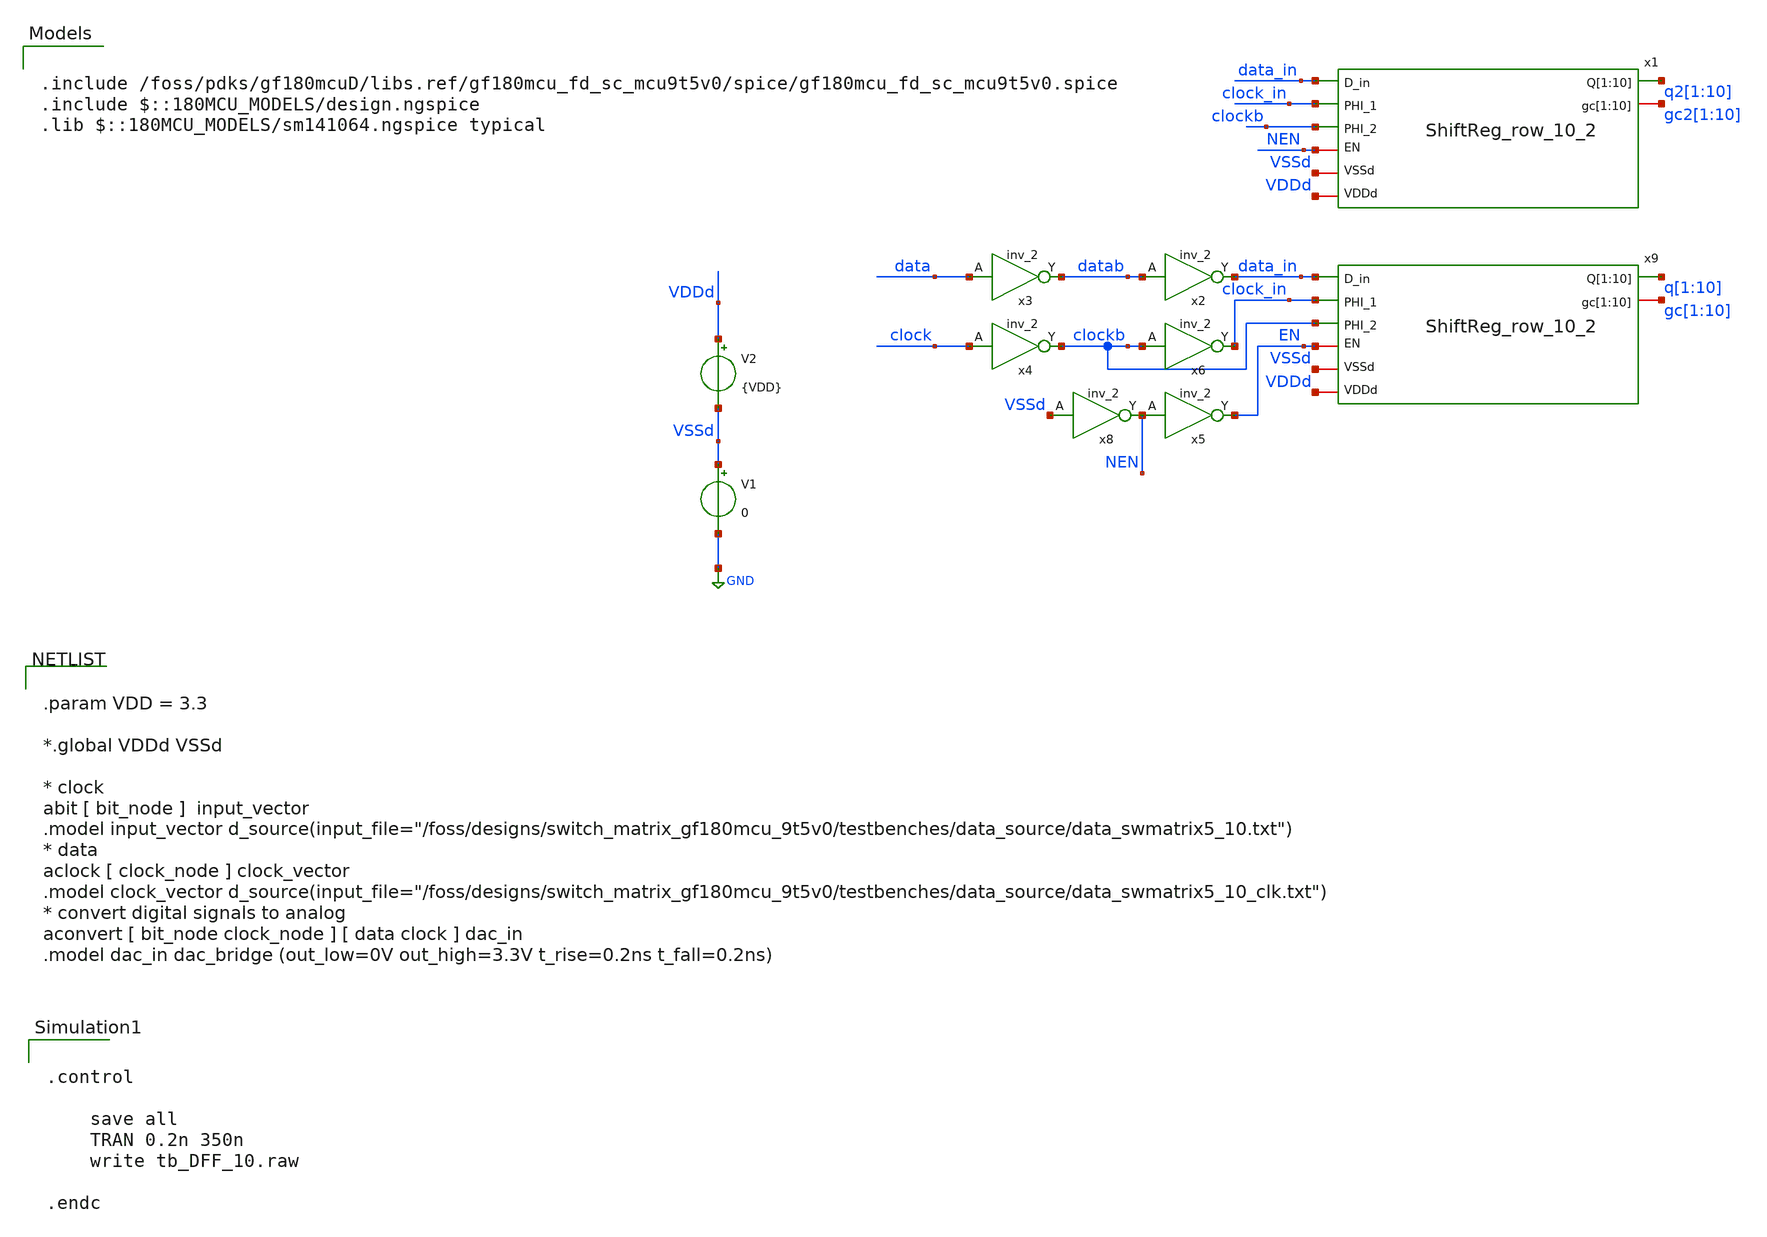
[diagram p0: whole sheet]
** sch_path: testbenches/tb_varioues/tb_DFF_10.sch
**.subckt tb_DFF_10
V1 VSSd GND 0
V2 VDDd VSSd {VDD}
x3 data VSSd VDDd VSSd VDDd datab gf180mcu_fd_sc_mcu9t5v0__inv_2
x2 datab VSSd VDDd VSSd VDDd data_in gf180mcu_fd_sc_mcu9t5v0__inv_2
x4 clock VSSd VDDd VSSd VDDd clockb gf180mcu_fd_sc_mcu9t5v0__inv_2
x5 NEN VSSd VDDd VSSd VDDd EN gf180mcu_fd_sc_mcu9t5v0__inv_2
x6 clockb VSSd VDDd VSSd VDDd clock_in gf180mcu_fd_sc_mcu9t5v0__inv_2
x8 VSSd VSSd VDDd VSSd VDDd NEN gf180mcu_fd_sc_mcu9t5v0__inv_2
x9 data_in q[1] q[2] q[3] q[4] q[5] q[6] q[7] q[8] q[9] q[10] gc[1] gc[2] gc[3] gc[4] gc[5] gc[6]
+ gc[7] gc[8] gc[9] gc[10] clock_in clockb EN VDDd VSSd ShiftReg_row_10_2
x1 data_in q2[1] q2[2] q2[3] q2[4] q2[5] q2[6] q2[7] q2[8] q2[9] q2[10] gc2[1] gc2[2] gc2[3] gc2[4]
+ gc2[5] gc2[6] gc2[7] gc2[8] gc2[9] gc2[10] clock_in clockb NEN VDDd VSSd ShiftReg_row_10_2
**** begin user architecture code

.include /foss/pdks/gf180mcuD/libs.ref/gf180mcu_fd_sc_mcu9t5v0/spice/gf180mcu_fd_sc_mcu9t5v0.spice
.include $::180MCU_MODELS/design.ngspice
.lib $::180MCU_MODELS/sm141064.ngspice typical



.param VDD = 3.3

*.global VDDd VSSd

* clock
abit [ bit_node ]  input_vector
.model input_vector
+ d_source(input_file="/foss/designs/switch_matrix_gf180mcu_9t5v0/testbenches/data_source/data_swmatrix5_10.txt")
* data
aclock [ clock_node ] clock_vector
.model clock_vector
+ d_source(input_file="/foss/designs/switch_matrix_gf180mcu_9t5v0/testbenches/data_source/data_swmatrix5_10_clk.txt")
* convert digital signals to analog
aconvert [ bit_node clock_node ] [ data clock ] dac_in
.model dac_in dac_bridge (out_low=0V out_high=3.3V t_rise=0.2ns t_fall=0.2ns)




.control

    save all
    TRAN 0.2n 350n
    write tb_DFF_10.raw

.endc


**** end user architecture code
**.ends
.GLOBAL GND
.end
